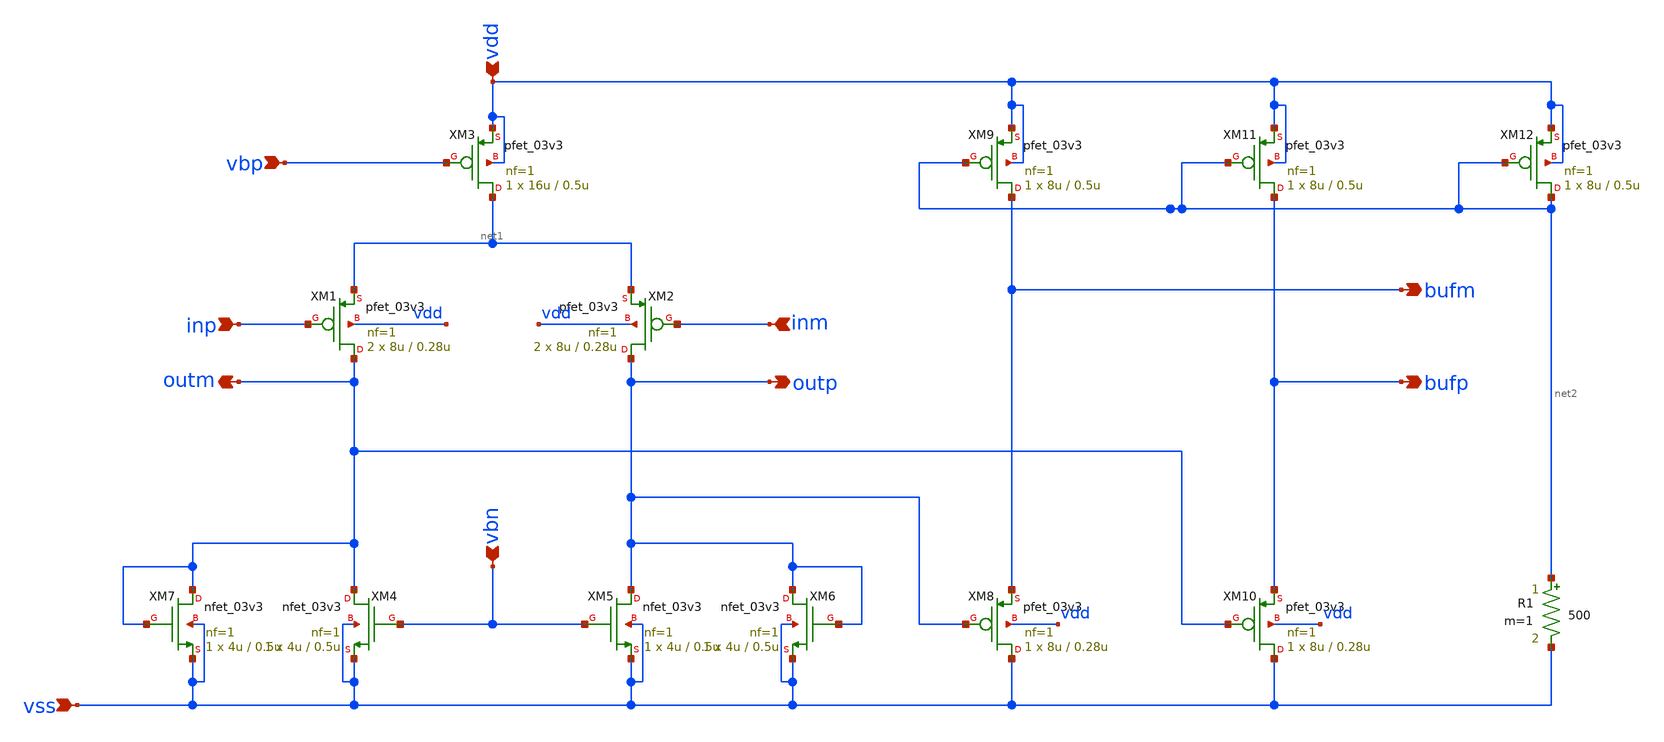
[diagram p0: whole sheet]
** sch_path: xschem/ring_osc_dly_p.sch
**.subckt ring_osc_dly_p inp inm outm outp vdd vbp vss vbn bufp bufm
*.ipin inp
*.ipin inm
*.opin outm
*.opin outp
*.ipin vdd
*.ipin vbp
*.ipin vss
*.ipin vbn
*.opin bufp
*.opin bufm
XM3 net1 vbp vdd vdd pfet_03v3 L=0.5u W=16u nf=1 ad='int((nf+1)/2) * W/nf * 0.18u' as='int((nf+2)/2) * W/nf * 0.18u'
+ pd='2*int((nf+1)/2) * (W/nf + 0.18u)' ps='2*int((nf+2)/2) * (W/nf + 0.18u)' nrd='0.18u / W' nrs='0.18u / W'
+ sa=0 sb=0 sd=0 m=1
XM1 outm inp net1 vdd pfet_03v3 L=0.28u W=8u nf=1 ad='int((nf+1)/2) * W/nf * 0.18u' as='int((nf+2)/2) * W/nf * 0.18u'
+ pd='2*int((nf+1)/2) * (W/nf + 0.18u)' ps='2*int((nf+2)/2) * (W/nf + 0.18u)' nrd='0.18u / W' nrs='0.18u / W'
+ sa=0 sb=0 sd=0 m=2
XM2 outp inm net1 vdd pfet_03v3 L=0.28u W=8u nf=1 ad='int((nf+1)/2) * W/nf * 0.18u' as='int((nf+2)/2) * W/nf * 0.18u'
+ pd='2*int((nf+1)/2) * (W/nf + 0.18u)' ps='2*int((nf+2)/2) * (W/nf + 0.18u)' nrd='0.18u / W' nrs='0.18u / W'
+ sa=0 sb=0 sd=0 m=2
XM4 outm vbn vss vss nfet_03v3 L=0.5u W=4u nf=1 ad='int((nf+1)/2) * W/nf * 0.18u' as='int((nf+2)/2) * W/nf * 0.18u'
+ pd='2*int((nf+1)/2) * (W/nf + 0.18u)' ps='2*int((nf+2)/2) * (W/nf + 0.18u)' nrd='0.18u / W' nrs='0.18u / W'
+ sa=0 sb=0 sd=0 m=1
XM5 outp vbn vss vss nfet_03v3 L=0.5u W=4u nf=1 ad='int((nf+1)/2) * W/nf * 0.18u' as='int((nf+2)/2) * W/nf * 0.18u'
+ pd='2*int((nf+1)/2) * (W/nf + 0.18u)' ps='2*int((nf+2)/2) * (W/nf + 0.18u)' nrd='0.18u / W' nrs='0.18u / W'
+ sa=0 sb=0 sd=0 m=1
XM6 outp outp vss vss nfet_03v3 L=0.5u W=4u nf=1 ad='int((nf+1)/2) * W/nf * 0.18u' as='int((nf+2)/2) * W/nf * 0.18u'
+ pd='2*int((nf+1)/2) * (W/nf + 0.18u)' ps='2*int((nf+2)/2) * (W/nf + 0.18u)' nrd='0.18u / W' nrs='0.18u / W'
+ sa=0 sb=0 sd=0 m=1
XM7 outm outm vss vss nfet_03v3 L=0.5u W=4u nf=1 ad='int((nf+1)/2) * W/nf * 0.18u' as='int((nf+2)/2) * W/nf * 0.18u'
+ pd='2*int((nf+1)/2) * (W/nf + 0.18u)' ps='2*int((nf+2)/2) * (W/nf + 0.18u)' nrd='0.18u / W' nrs='0.18u / W'
+ sa=0 sb=0 sd=0 m=1
XM9 bufm net2 vdd vdd pfet_03v3 L=0.5u W=8u nf=1 ad='int((nf+1)/2) * W/nf * 0.18u' as='int((nf+2)/2) * W/nf * 0.18u'
+ pd='2*int((nf+1)/2) * (W/nf + 0.18u)' ps='2*int((nf+2)/2) * (W/nf + 0.18u)' nrd='0.18u / W' nrs='0.18u / W'
+ sa=0 sb=0 sd=0 m=1
XM11 bufp net2 vdd vdd pfet_03v3 L=0.5u W=8u nf=1 ad='int((nf+1)/2) * W/nf * 0.18u' as='int((nf+2)/2) * W/nf * 0.18u'
+ pd='2*int((nf+1)/2) * (W/nf + 0.18u)' ps='2*int((nf+2)/2) * (W/nf + 0.18u)' nrd='0.18u / W' nrs='0.18u / W'
+ sa=0 sb=0 sd=0 m=1
XM8 vss outp bufm vdd pfet_03v3 L=0.28u W=8u nf=1 ad='int((nf+1)/2) * W/nf * 0.18u' as='int((nf+2)/2) * W/nf * 0.18u'
+ pd='2*int((nf+1)/2) * (W/nf + 0.18u)' ps='2*int((nf+2)/2) * (W/nf + 0.18u)' nrd='0.18u / W' nrs='0.18u / W'
+ sa=0 sb=0 sd=0 m=1
XM10 vss outm bufp vdd pfet_03v3 L=0.28u W=8u nf=1 ad='int((nf+1)/2) * W/nf * 0.18u' as='int((nf+2)/2) * W/nf * 0.18u'
+ pd='2*int((nf+1)/2) * (W/nf + 0.18u)' ps='2*int((nf+2)/2) * (W/nf + 0.18u)' nrd='0.18u / W' nrs='0.18u / W'
+ sa=0 sb=0 sd=0 m=1
XM12 net2 net2 vdd vdd pfet_03v3 L=0.5u W=8u nf=1 ad='int((nf+1)/2) * W/nf * 0.18u' as='int((nf+2)/2) * W/nf * 0.18u'
+ pd='2*int((nf+1)/2) * (W/nf + 0.18u)' ps='2*int((nf+2)/2) * (W/nf + 0.18u)' nrd='0.18u / W' nrs='0.18u / W'
+ sa=0 sb=0 sd=0 m=1
R1 net2 vss 500 m=1
**.ends
.end
